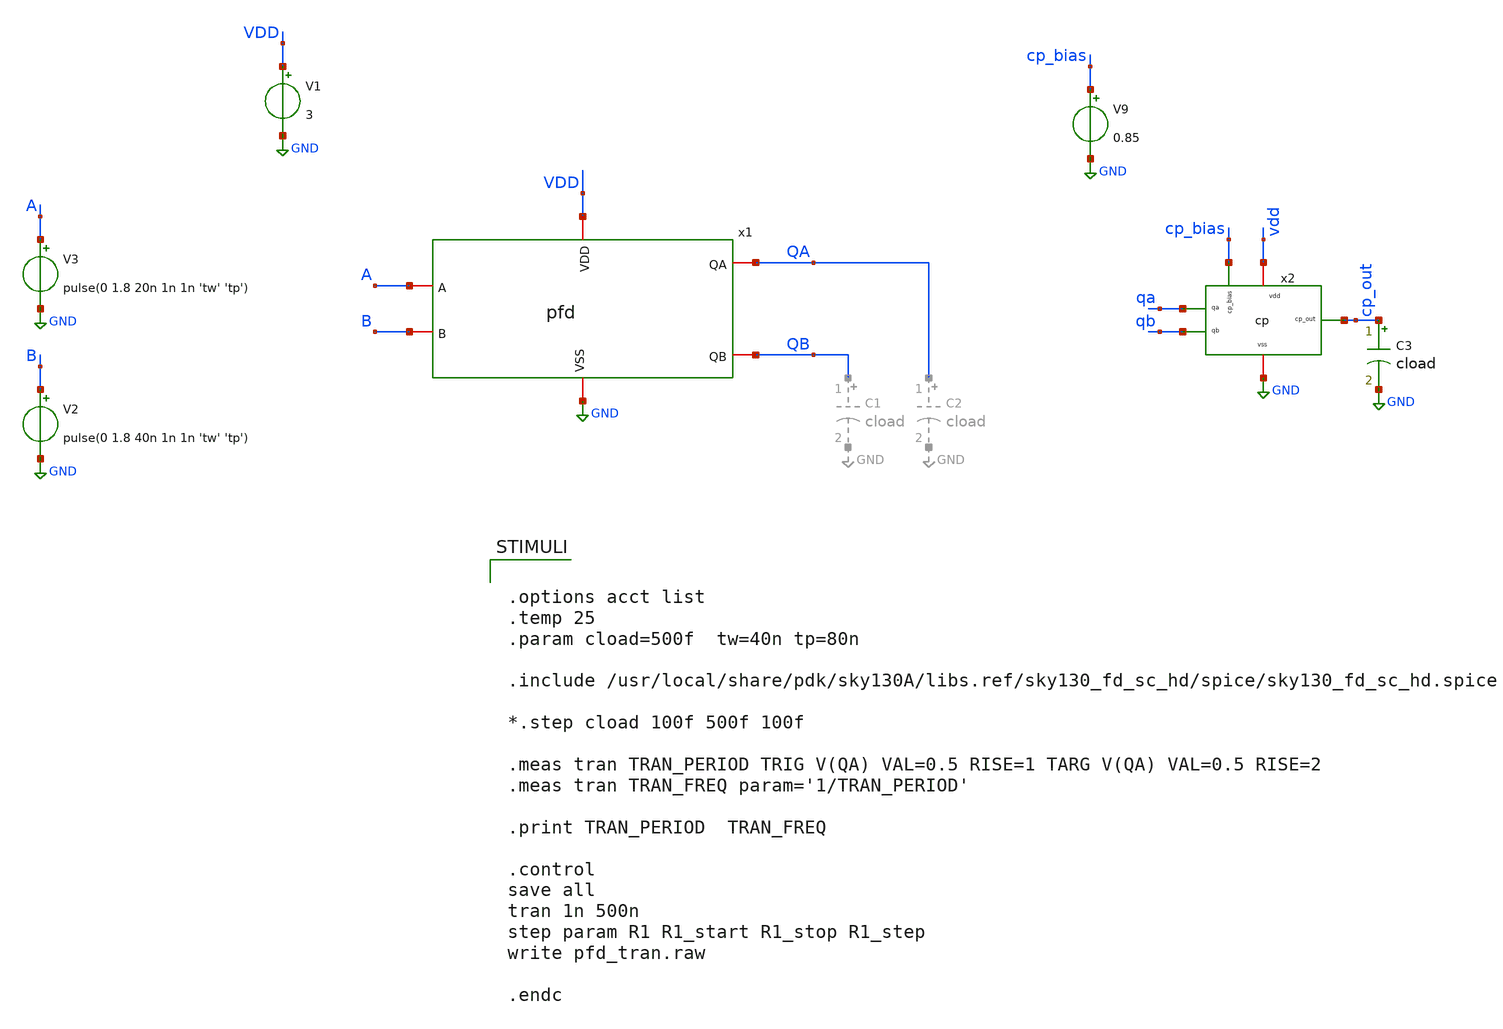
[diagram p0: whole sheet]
** sch_path: xschem01/untitled.sch
**.subckt untitled
x1 GND VDD A QA QB B pfd
V1 VDD GND 3
V2 B GND pulse(0 1.8 40n 1n 1n 'tw' 'tp')
V3 A GND pulse(0 1.8 20n 1n 1n 'tw' 'tp')
x2 vdd qa cp_out qb GND cp_bias cp
C3 cp_out GND cload m=1
V9 cp_bias GND 0.85
**** begin user architecture code


.options acct list
.temp 25
.param cload=500f  tw=40n tp=80n

.include /usr/local/share/pdk/sky130A/libs.ref/sky130_fd_sc_hd/spice/sky130_fd_sc_hd.spice

*.step cload 100f 500f 100f

.meas tran TRAN_PERIOD TRIG V(QA) VAL=0.5 RISE=1 TARG V(QA) VAL=0.5 RISE=2
.meas tran TRAN_FREQ param='1/TRAN_PERIOD'

.print TRAN_PERIOD  TRAN_FREQ

.control
save all
tran 1n 500n
step param R1 R1_start R1_stop R1_step
write pfd_tran.raw

.endc



** opencircuitdesign pdks install
.lib $::SKYWATER_MODELS/sky130.lib.spice tt




.options acct list savecurrents
.temp 25
.param cload=5p  ibias=10u  low=0  high=1.8  tw=40n  tp=80n
******charging
*+ tw_a=50n tp_a=80n
*+ tw_b=0n  tp_b=0n
******discharging
*+ tw_a=0n tp_a=0n
*+ tw_b=50n  tp_b=80n

.include /usr/local/share/pdk/sky130A/libs.ref/sky130_fd_sc_hd/spice/sky130_fd_sc_hd.spice

.ic v(cp_out)=1.8  v(cp_out1)=1.8

*.meas tran TRAN_PERIOD TRIG V(QA) VAL=0.5 RISE=1 TARG V(QA) VAL=0.5 RISE=2
*.meas tran TRAN_FREQ param='1/TRAN_PERIOD'

.print TRAN_PERIOD  TRAN_FREQ
*print @m.x1.xm3.msky130_fd_pr__nfet_01v8[id]  @m.x1.xm4.msky130_fd_pr__pfet_01v8[id]


.control
save all
save @m.x1.xm3.msky130_fd_pr__nfet_01v8[vth]
save @m.x1.xm3.msky130_fd_pr__nfet_01v8[vgs]
save @m.x1.xm3.msky130_fd_pr__nfet_01v8[gm]

save @m.x1.xm6.msky130_fd_pr__pfet_01v8[vth]

save @m.x1.xm4.msky130_fd_pr__pfet_01v8[vsg]
save @m.x1.xm6.msky130_fd_pr__pfet_01v8[vsg]


op
write cp_tran.raw
set appendwrite

tran 1n 10u
write cp_tran.raw

print  @m.x1.xm3.msky130_fd_pr__nfet_01v8[vth]
print  @m.x1.xm3.msky130_fd_pr__nfet_01v8[gm]
print  @m.x1.xm3.msky130_fd_pr__nfet_01v8[vgs]

*print x1.bias  x1.n1   x1.cp_out

.endc


**** end user architecture code
**.ends
.GLOBAL GND
.end
